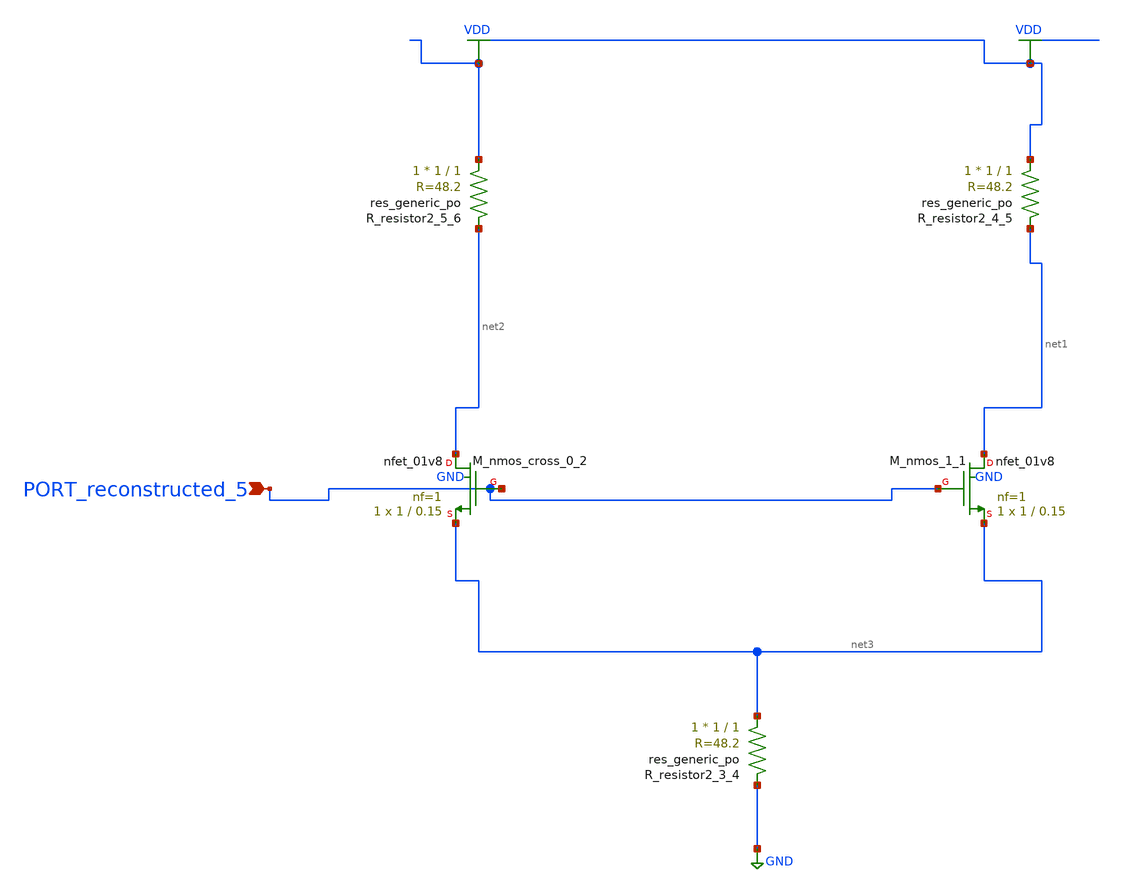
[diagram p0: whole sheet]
** sch_path: schematics/AMSNet/218.sch
**.subckt 218 PORT_reconstructed_5
*.ipin PORT_reconstructed_5
XM_nmos_1_1 net1 PORT_reconstructed_5 net3 GND sky130_fd_pr__nfet_01v8 L=0.15 W=1 nf=1 ad='int((1 + 1)/2) * 1 / 1 * 0.29'
+ as='int((1 + 2)/2) * 1 / 1 * 0.29' pd='2*int((1 + 1)/2) * (1 / 1 + 0.29)' ps='2*int((1 + 2)/2) * (1 / 1 + 0.29)'
+ nrd='0.29 / 1 ' nrs='0.29 / 1 ' sa=0 sb=0 sd=0 mult=1 m=1
XM_nmos_cross_0_2 net2 PORT_reconstructed_5 net3 GND sky130_fd_pr__nfet_01v8 L=0.15 W=1 nf=1 ad='int((1 + 1)/2) * 1 / 1 * 0.29'
+ as='int((1 + 2)/2) * 1 / 1 * 0.29' pd='2*int((1 + 1)/2) * (1 / 1 + 0.29)' ps='2*int((1 + 2)/2) * (1 / 1 + 0.29)'
+ nrd='0.29 / 1 ' nrs='0.29 / 1 ' sa=0 sb=0 sd=0 mult=1 m=1
XR_resistor2_3_4 net3 GND sky130_fd_pr__res_generic_po W=1 L=1 m=1
XR_resistor2_4_5 VDD net1 sky130_fd_pr__res_generic_po W=1 L=1 m=1
XR_resistor2_5_6 VDD net2 sky130_fd_pr__res_generic_po W=1 L=1 m=1
**.ends
.GLOBAL GND
.GLOBAL VDD
.end
